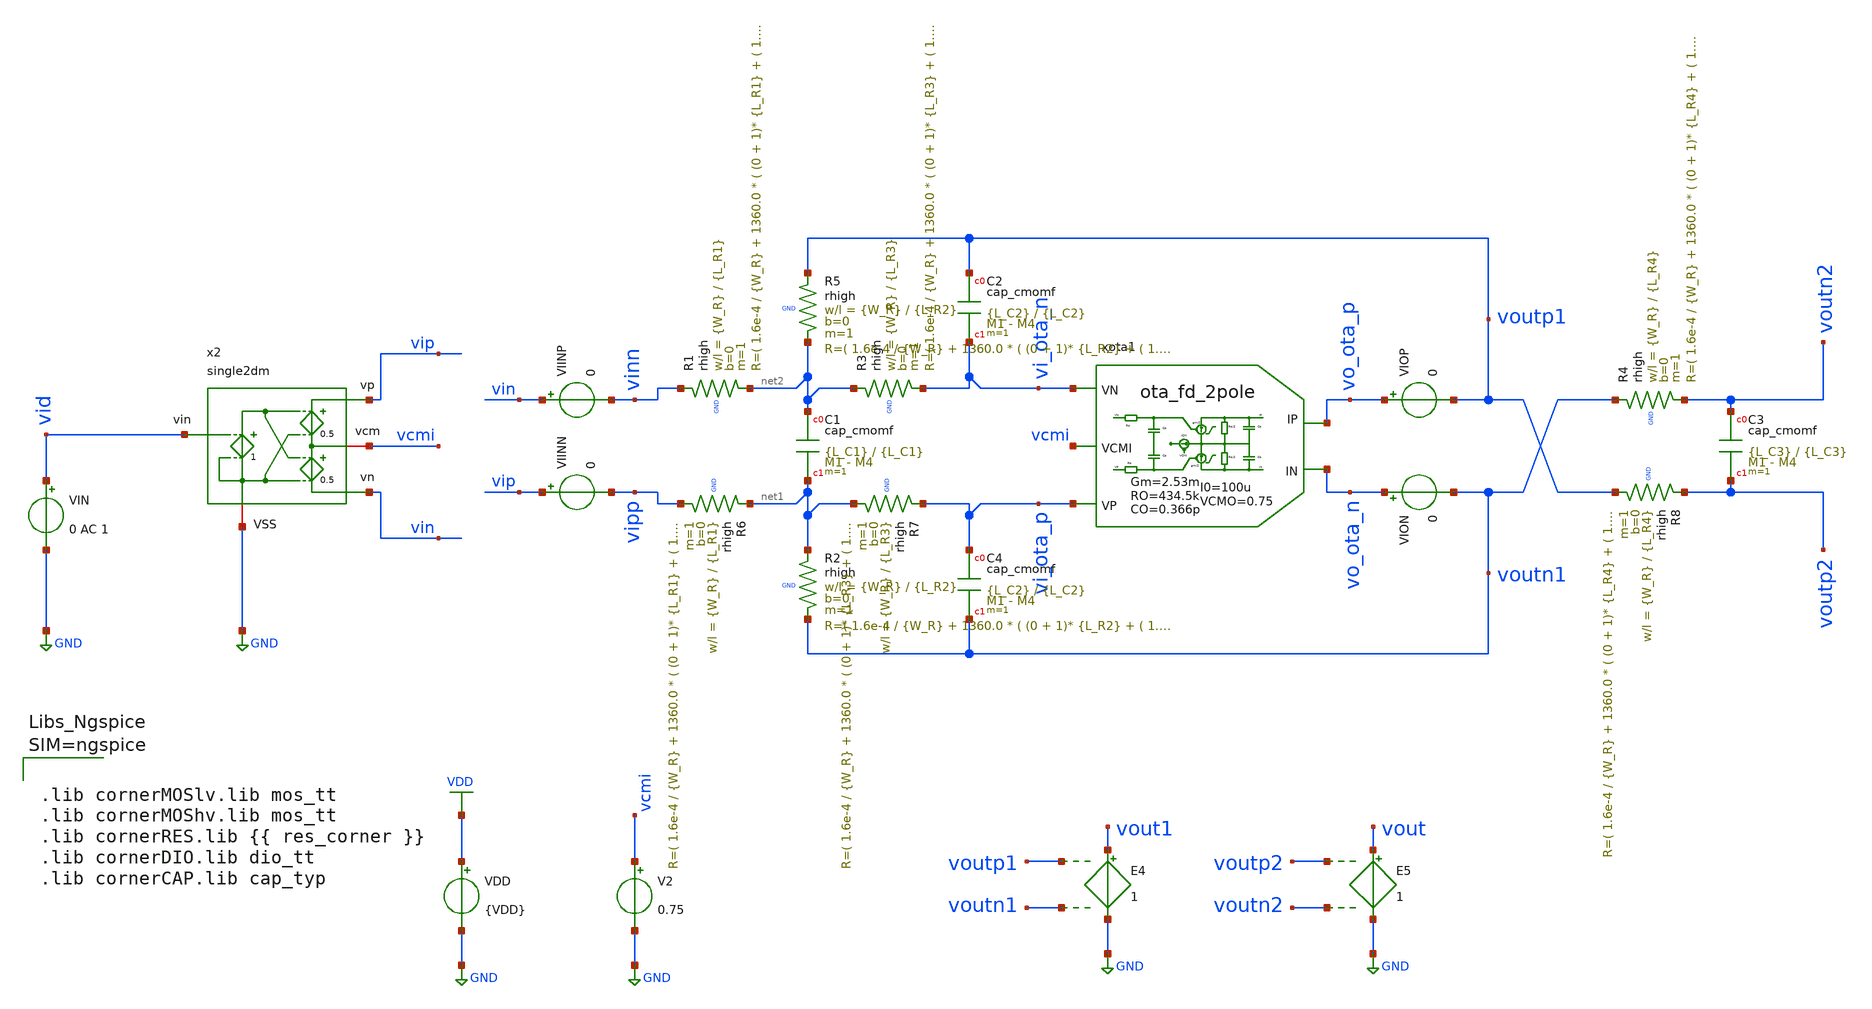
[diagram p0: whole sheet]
** sch_path: macros/filter_cmos5l/testbenches/xschem/filter_cl_ideal.sch
**.subckt filter_cl_ideal
VIN vid GND 0 AC 1
E4 vout1 GND voutp1 voutn1 1
VIINP vin vinn 0
VIINN vip vipp 0
E5 vout GND voutp2 voutn2 1
VIOP vo_ota_p voutp1 0
VION vo_ota_n voutn1 0
VDD VDD GND {VDD}
x2 vip vid vcmi GND vin single2dm
V2 vcmi GND 0.75
xota1 vi_ota_n vo_ota_p vo_ota_n vi_ota_p vcmi ota_fd_2pole GM=2.53m RO=434.5k CO=0.366p RP=0
+ CP=0.1p VCMO=0.75 I0=100u
XR5 voutp1 net2 GND rhigh w={W_R} l={L_R2} m=1 b=0 mm_ok=1
XR2 net1 voutn1 GND rhigh w={W_R} l={L_R2} m=1 b=0 mm_ok=1
XR1 vinn net2 GND rhigh w={W_R} l={L_R1} m=1 b=0 mm_ok=1
XR6 net1 vipp GND rhigh w={W_R} l={L_R1} m=1 b=0 mm_ok=1
XR7 vi_ota_p net1 GND rhigh w={W_R} l={L_R3} m=1 b=0 mm_ok=1
XR3 net2 vi_ota_n GND rhigh w={W_R} l={L_R3} m=1 b=0 mm_ok=1
XR4 voutn1 voutn2 GND rhigh w={W_R} l={L_R4} m=1 b=0 mm_ok=1
XR8 voutp2 voutp1 GND rhigh w={W_R} l={L_R4} m=1 b=0 mm_ok=1
XC1 net2 net1 cap_cmomf w={L_C1} l={L_C1} mmin=1 mmax=4 subblock=0 rfmodel=0 subscale=1 m=1 mm_ok=1
XC2 voutp1 vi_ota_n cap_cmomf w={L_C2} l={L_C2} mmin=1 mmax=4 subblock=0 rfmodel=0 subscale=1 m=1 mm_ok=1
XC4 vi_ota_p voutn1 cap_cmomf w={L_C2} l={L_C2} mmin=1 mmax=4 subblock=0 rfmodel=0 subscale=1 m=1 mm_ok=1
XC3 voutn2 voutp2 cap_cmomf w={L_C3} l={L_C3} mmin=1 mmax=4 subblock=0 rfmodel=0 subscale=1 m=1 mm_ok=1
**** begin user architecture code


.include /foss/designs/kvosid_336004_ss26/macros/filter_cmos5l/scripts/sizing/filterPassives.spice
.include /foss/designs/kvosid_336004_ss26/macros/filter_cmos5l/scripts/sizing/filterPassivesSizing.spice
.param VDD = {{ VDD }}
.options savecurrents
.options method=gear reltol=.005
.options sparse
.control

let f_min = 10
let f_max = 100Meg
let f_stop = 9Meg
let f_nmin = 100
let f_nmax = 5Meg

let n_bits = 8
let Adc = 10
let v_fs = 1.0
let v_lsb = v_fs/2^n_bits
let v_qn = v_lsb/sqrt(12)
let err_gain_spec = v_lsb/v_fs
let vo_n_max = 113e-6

let v_step_o = v_fs
let v_step_i = v_step_o/Adc

let t_rf = 0.1u
let t_step = 50u
let t_delay = 0
let t_per = 2*t_step

let tstep = 0.1*t_rf
let tstop = 2*t_per
let tstart = t_delay

op
ac dec 100 $&const.f_min $&const.f_max
let acgain=vout
tran $&tstep $&tstop $&tstart

quit
.endc




.lib cornerMOSlv.lib mos_tt
.lib cornerMOShv.lib mos_tt
.lib cornerRES.lib {{ res_corner }}
.lib cornerDIO.lib dio_tt
.lib cornerCAP.lib cap_typ



**** end user architecture code
**.ends

* expanding   symbol:  single2dm.sym # of pins=5
** sym_path: single2dm.sym
** sch_path: single2dm.sch
.subckt single2dm vp vin vcm VSS vn
*.ipin vin
*.opin vn
*.iopin vcm
*.opin vp
*.iopin VSS
E3 vcm vn net1 VSS 0.5
E2 vp vcm net1 VSS 0.5
E1 net1 VSS vin VSS 1
.ends


* expanding   symbol:  ota_fd_2pole.sym # of pins=5
** sym_path: ota_fd_2pole.sym
** sch_path: ota_fd_2pole.sch
.subckt ota_fd_2pole VN IP IN VP VCMI  GM=1u RO=100Meg CO=1p RP=0 CP=0.1p VCMO=0 I0=1u
*.ipin VP
*.ipin VN
*.opin IP
*.opin IN
*.ipin VCMI
R3 IP net1 {RO/2} m=1
R4 IN net1 {RO/2} m=1
C3 IP net1 {CO} m=1
R5 VN ip1 {RP} m=1
C4 ip1 VCMI {CP} m=1
C6 in1 VCMI {CP} m=1
C8 IN net1 {CO} m=1
R7 VP in1 {RP} m=1
B2 IP net1 I = {I0*tanh(GM/2*V(ip1,in1)/I0)}
B1 net1 IN I = {I0*tanh(GM/2*V(ip1,in1)/I0)}
B5 net1 GND I = {VCMO-(V(IP)+V(IN))/2}
.ends

.GLOBAL GND
.GLOBAL VDD
.end
